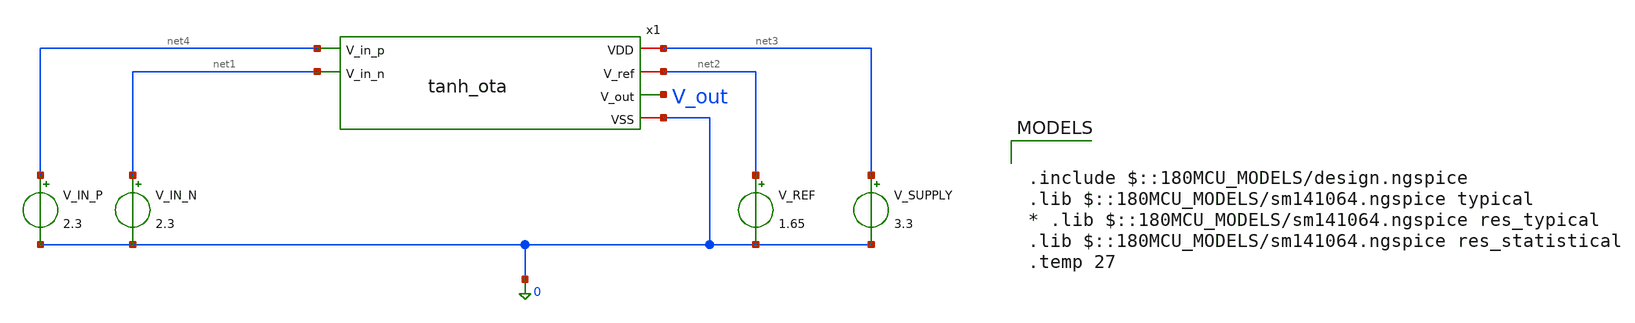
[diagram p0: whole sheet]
** sch_path: schematics/tb_tanh_ota.sch
**.subckt tb_tanh_ota
x1 net3 net2 V_out net4 net1 0 tanh_ota
V_REF net2 0 1.65
V_SUPPLY net3 0 3.3
V_IN_N net1 0 2.3
V_IN_P net4 0 2.3
**** begin user architecture code

.include $::180MCU_MODELS/design.ngspice
.lib $::180MCU_MODELS/sm141064.ngspice typical
* .lib $::180MCU_MODELS/sm141064.ngspice res_typical
.lib $::180MCU_MODELS/sm141064.ngspice res_statistical
.temp 27



.control
  op
  echo "--- tanh OTA x1: transistor op points ---"
  print @m.x1.xm1.m0[vgs] @m.x1.xm1.m0[vth] @m.x1.xm1.m0[vdsat] @m.x1.xm1.m0[id] @m.x1.xm1.m0[gm]
+ @m.x1.xm1.m0[gds]
  print @m.x1.xm2.m0[vgs] @m.x1.xm2.m0[vth] @m.x1.xm2.m0[vdsat] @m.x1.xm2.m0[id] @m.x1.xm2.m0[gm]
+ @m.x1.xm2.m0[gds]
  print @m.x1.xm3.m0[vgs] @m.x1.xm3.m0[vth] @m.x1.xm3.m0[vdsat] @m.x1.xm3.m0[id] @m.x1.xm3.m0[gm]
+ @m.x1.xm3.m0[gds]
  print @m.x1.xm4.m0[vgs] @m.x1.xm4.m0[vth] @m.x1.xm4.m0[vdsat] @m.x1.xm4.m0[id] @m.x1.xm4.m0[gm]
+ @m.x1.xm4.m0[gds]
  print @m.x1.xm5.m0[vgs] @m.x1.xm5.m0[vth] @m.x1.xm5.m0[vdsat] @m.x1.xm5.m0[id] @m.x1.xm5.m0[gm]
+ @m.x1.xm5.m0[gds]
  echo "--- tanh OTA x1: reference resistor ---"
  print @r.x1.xr1.rt1[resistance] @r.x1.xr1.rt2[resistance]
  dc V_IN_P 2.1 2.5 0.002
  let V_out = v(V_out)
  plot V_out title "tanh OTA: Saturating Transfer Characteristic"
  wrdata /foss/designs/analog-perceptron-gf180mcu/plots/tanh_ota_sweep.txt V_out
  * === OP-SWEEP DIAGNOSTIC: all 5 devices' headroom across full input range ===
  save all @m.x1.xm1.m0[vgs] @m.x1.xm1.m0[vth] @m.x1.xm1.m0[vdsat] @m.x1.xm1.m0[id] @m.x1.xm1.m0[gm] @m.x1.xm1.m0[gds] @m.x1.xm2.m0[vgs] @m.x1.xm2.m0[vth] @m.x1.xm2.m0[vdsat] @m.x1.xm2.m0[id] @m.x1.xm2.m0[gm] @m.x1.xm2.m0[gds] @m.x1.xm3.m0[vgs] @m.x1.xm3.m0[vth] @m.x1.xm3.m0[vdsat] @m.x1.xm3.m0[id] @m.x1.xm3.m0[gm] @m.x1.xm3.m0[gds] @m.x1.xm4.m0[vgs] @m.x1.xm4.m0[vth] @m.x1.xm4.m0[vdsat] @m.x1.xm4.m0[id] @m.x1.xm4.m0[gm] @m.x1.xm4.m0[gds] @m.x1.xm5.m0[vgs] @m.x1.xm5.m0[vth] @m.x1.xm5.m0[vdsat] @m.x1.xm5.m0[id] @m.x1.xm5.m0[gm] @m.x1.xm5.m0[gds]
  dc V_IN_P 2.1 2.5 0.002
  wrdata /foss/designs/analog-perceptron-gf180mcu/plots/opsweep_tanh_ota.txt v(V_out) @m.x1.xm1.m0[vgs] @m.x1.xm1.m0[vth] @m.x1.xm1.m0[vdsat] @m.x1.xm1.m0[id] @m.x1.xm1.m0[gm] @m.x1.xm1.m0[gds] @m.x1.xm2.m0[vgs] @m.x1.xm2.m0[vth] @m.x1.xm2.m0[vdsat] @m.x1.xm2.m0[id] @m.x1.xm2.m0[gm] @m.x1.xm2.m0[gds] @m.x1.xm3.m0[vgs] @m.x1.xm3.m0[vth] @m.x1.xm3.m0[vdsat] @m.x1.xm3.m0[id] @m.x1.xm3.m0[gm] @m.x1.xm3.m0[gds] @m.x1.xm4.m0[vgs] @m.x1.xm4.m0[vth] @m.x1.xm4.m0[vdsat] @m.x1.xm4.m0[id] @m.x1.xm4.m0[gm] @m.x1.xm4.m0[gds] @m.x1.xm5.m0[vgs] @m.x1.xm5.m0[vth] @m.x1.xm5.m0[vdsat] @m.x1.xm5.m0[id] @m.x1.xm5.m0[gm] @m.x1.xm5.m0[gds]
.endc


**** end user architecture code
**.ends

* expanding   symbol:  analog-perceptron-gf180mcu/schematics/tanh_ota.sym # of pins=6
** sym_path: schematics/tanh_ota.sym
** sch_path: schematics/tanh_ota.sch
.subckt tanh_ota VDD V_ref V_out V_in_p V_in_n VSS
*.iopin VDD
*.iopin VSS
*.ipin V_in_p
*.ipin V_in_n
*.opin V_out
*.iopin V_ref
XM1 net2 V_in_p net1 VSS nfet_03v3 L=0.5u W=10u nf=1 ad='int((nf+1)/2) * W/nf * 0.18u' as='int((nf+2)/2)
+ * W/nf * 0.18u' pd='2*int((nf+1)/2) * (W/nf + 0.18u)' ps='2*int((nf+2)/2) * (W/nf + 0.18u)' nrd='0.18u
+ / W' nrs='0.18u / W' sa=0 sb=0 sd=0 m=1
XM2 V_out V_in_n net1 VSS nfet_03v3 L=0.5u W=10u nf=1 ad='int((nf+1)/2) * W/nf * 0.18u' as='int((nf+2)/2)
+ * W/nf * 0.18u' pd='2*int((nf+1)/2) * (W/nf + 0.18u)' ps='2*int((nf+2)/2) * (W/nf + 0.18u)' nrd='0.18u
+ / W' nrs='0.18u / W' sa=0 sb=0 sd=0 m=1
XM3 net1 net3 VSS VSS nfet_03v3 L=0.5u W=3u nf=1 ad='int((nf+1)/2) * W/nf * 0.18u' as='int((nf+2)/2)
+ * W/nf * 0.18u' pd='2*int((nf+1)/2) * (W/nf + 0.18u)' ps='2*int((nf+2)/2) * (W/nf + 0.18u)' nrd='0.18u
+ / W' nrs='0.18u / W' sa=0 sb=0 sd=0 m=1
XM4 net2 net2 VDD VDD pfet_03v3 L=0.5u W=20u nf=1 ad='int((nf+1)/2) * W/nf * 0.18u' as='int((nf+2)/2)
+ * W/nf * 0.18u' pd='2*int((nf+1)/2) * (W/nf + 0.18u)' ps='2*int((nf+2)/2) * (W/nf + 0.18u)' nrd='0.18u
+ / W' nrs='0.18u / W' sa=0 sb=0 sd=0 m=1
XM5 V_out net2 VDD VDD pfet_03v3 L=0.5u W=20u nf=1 ad='int((nf+1)/2) * W/nf * 0.18u' as='int((nf+2)/2)
+ * W/nf * 0.18u' pd='2*int((nf+1)/2) * (W/nf + 0.18u)' ps='2*int((nf+2)/2) * (W/nf + 0.18u)' nrd='0.18u
+ / W' nrs='0.18u / W' sa=0 sb=0 sd=0 m=1
XR6 V_out V_ref VSS ppolyf_u_1k r_width=3e-6 r_length=45e-6 m=1
XM6 net3 net3 VSS VSS nfet_03v3 L=0.5u W=30u nf=1 ad='int((nf+1)/2) * W/nf * 0.18u' as='int((nf+2)/2)
+ * W/nf * 0.18u' pd='2*int((nf+1)/2) * (W/nf + 0.18u)' ps='2*int((nf+2)/2) * (W/nf + 0.18u)' nrd='0.18u
+ / W' nrs='0.18u / W' sa=0 sb=0 sd=0 m=1
XR1 net3 VDD VSS ppolyf_u_1k r_width=3e-6 r_length=110e-6 m=1
.ends

.end
